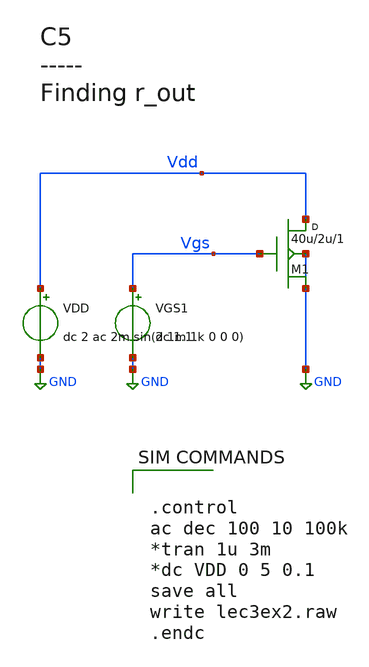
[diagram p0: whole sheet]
** sch_path: lec3ex2.sch
**.subckt lec3ex2
M1 Vdd Vgs GND GND NMOS w=40u l=2u m=1
VGS1 Vgs GND dc 1.1
VDD Vdd GND dc 2 ac 2m sin(2 1m 1k 0 0 0)
**** begin user architecture code


.control
ac dec 100 10 100k
*tran 1u 3m
*dc VDD 0 5 0.1
save all
write lec3ex2.raw
.endc




*

* Long channel models from CMOS Circuit Design, Layout, and Simulation,

* Level=3 models VDD=5V, see CMOSedu.com

*

.MODEL N_1u NMOS LEVEL  = 3
  TOX    = 200E-10         NSUB   = 1E17            GAMMA  = 0.5
  PHI    = 0.7             VTO    = 0.8             DELTA  = 3.0
  UO     = 650             ETA    = 3.0E-6          THETA  = 0.1
  KP     = 120E-6          VMAX   = 1E5             KAPPA  = 0.3
  RSH    = 0               NFS    = 1E12            TPG    = 1
  XJ     = 500E-9          LD     = 100E-9
  CGDO   = 200E-12         CGSO   = 200E-12         CGBO   = 1E-10
  CJ     = 400E-6          PB     = 1               MJ     = 0.5
  CJSW   = 300E-12         MJSW   = 0.5

*

.MODEL P_1u PMOS LEVEL  = 3
  TOX    = 200E-10         NSUB   = 1E17            GAMMA  = 0.6
  PHI    = 0.7             VTO    = -0.9            DELTA  = 0.1
  UO     = 250             ETA    = 0               THETA  = 0.1
  KP     = 40E-6           VMAX   = 5E4             KAPPA  = 1
  RSH    = 0               NFS    = 1E12            TPG    = -1
  XJ     = 500E-9          LD     = 100E-9
  CGDO   = 200E-12         CGSO   = 200E-12         CGBO   = 1E-10
  CJ     = 400E-6          PB     = 1               MJ     = 0.5
  CJSW   = 300E-12         MJSW   = 0.5

*

*

* Short channel models from CMOS Circuit Design, Layout, and Simulation,

* 50nm BSIM4 models VDD=1V, see CMOSedu.com

*

.model  N_50n  nmos  level = 54
 binunit = 1            paramchk= 1            mobmod  = 0
 capmod  = 2            igcmod  = 1            igbmod  = 1            geomod  = 0
 diomod  = 1            rdsmod  = 0            rbodymod= 1            rgatemod= 1
 permod  = 1            acnqsmod= 0            trnqsmod= 0
 tnom    = 27           toxe    = 1.4e-009     toxp    = 7e-010       toxm    = 1.4e-009
 epsrox  = 3.9          wint    = 5e-009       lint    = 1.2e-008
 ll      = 0            wl      = 0            lln     = 1            wln     = 1
 lw      = 0            ww      = 0            lwn     = 1            wwn     = 1
 lwl     = 0            wwl     = 0            xpart   = 0            toxref  = 1.4e-009
 vth0    = 0.22         k1      = 0.35         k2      = 0.05         k3      = 0
 k3b     = 0            w0      = 2.5e-006     dvt0    = 2.8          dvt1    = 0.52
 dvt2    = -0.032       dvt0w   = 0            dvt1w   = 0            dvt2w   = 0
 dsub    = 2            minv    = 0.05         voffl   = 0            dvtp0   = 1e-007
 dvtp1   = 0.05         lpe0    = 5.75e-008    lpeb    = 2.3e-010     xj      = 2e-008
 ngate   = 5e+020       ndep    = 2.8e+018     nsd     = 1e+020       phin    = 0
 cdsc    = 0.0002       cdscb   = 0            cdscd   = 0            cit     = 0
 voff    = -0.15        nfactor = 1.2          eta0    = 0.15         etab    = 0
 vfb     = -0.55        u0      = 0.032        ua      = 1.6e-010     ub      = 1.1e-017
 uc      = -3e-011      vsat    = 1.1e+005     a0      = 2            ags     = 1e-020
 a1      = 0            a2      = 1            b0      = -1e-020      b1      = 0
 keta    = 0.04         dwg     = 0            dwb     = 0            pclm    = 0.18
 pdiblc1 = 0.028        pdiblc2 = 0.022        pdiblcb = -0.005       drout   = 0.45
 pvag    = 1e-020       delta   = 0.01         pscbe1  = 8.14e+008    pscbe2  = 1e-007
 fprout  = 0.2          pdits   = 0.2          pditsd  = 0.23         pditsl  = 2.3e+006
 rsh     = 3            rdsw    = 150          rsw     = 150          rdw     = 150
 rdswmin = 0            rdwmin  = 0            rswmin  = 0            prwg    = 0
 prwb    = 6.8e-011     wr      = 1            alpha0  = 0.074        alpha1  = 0.005
 beta0   = 30           agidl   = 0.0002       bgidl   = 2.1e+009     cgidl   = 0.0002
 egidl   = 0.8
 aigbacc = 0.012        bigbacc = 0.0028       cigbacc = 0.002
 nigbacc = 1            aigbinv = 0.014        bigbinv = 0.004        cigbinv = 0.004
 eigbinv = 1.1          nigbinv = 3            aigc    = 0.017        bigc    = 0.0028
 cigc    = 0.002        aigsd   = 0.017        bigsd   = 0.0028       cigsd   = 0.002
 nigc    = 1            poxedge = 1            pigcd   = 1            ntox    = 1
 xrcrg1  = 12           xrcrg2  = 5
 cgso    = 6.238e-010   cgdo    = 6.238e-010   cgbo    = 2.56e-011    cgdl    = 2.495e-10
 cgsl    = 2.495e-10    ckappas = 0.02         ckappad = 0.02         acde    = 1
 moin    = 15           noff    = 0.9          voffcv  = 0.02
 kt1     = -0.21        kt1l    = 0.0           kt2     = -0.042        ute     = -1.5
 ua1     = 1e-009       ub1     = -3.5e-019     uc1     = 0             prt     = 0
 at      = 53000
 fnoimod = 1            tnoimod = 0
 jss     = 0.0001       jsws    = 1e-011       jswgs   = 1e-010       njs     = 1
 ijthsfwd= 0.01         ijthsrev= 0.001        bvs     = 10           xjbvs   = 1
 jsd     = 0.0001       jswd    = 1e-011       jswgd   = 1e-010       njd     = 1
 ijthdfwd= 0.01         ijthdrev= 0.001        bvd     = 10           xjbvd   = 1
 pbs     = 1            cjs     = 0.0005       mjs     = 0.5          pbsws   = 1
 cjsws   = 5e-010       mjsws   = 0.33         pbswgs  = 1            cjswgs  = 5e-010
 mjswgs  = 0.33         pbd     = 1            cjd     = 0.0005       mjd     = 0.5
 pbswd   = 1            cjswd   = 5e-010       mjswd   = 0.33         pbswgd  = 1
 cjswgd  = 5e-010       mjswgd  = 0.33         tpb     = 0.005        tcj     = 0.001
 tpbsw   = 0.005        tcjsw   = 0.001        tpbswg  = 0.005        tcjswg  = 0.001
 xtis    = 3            xtid    = 3
 dmcg    = 0e-006       dmci    = 0e-006       dmdg    = 0e-006       dmcgt   = 0e-007
 dwj     = 0e-008     	xgw     = 0e-007       xgl     = 0e-008
 rshg    = 0.4          gbmin   = 1e-010       rbpb    = 5            rbpd    = 15
 rbps    = 15           rbdb    = 15           rbsb    = 15           ngcon   = 1

*

.model  P_50n  pmos  level = 54
 binunit = 1            paramchk= 1            mobmod  = 0
 capmod  = 2            igcmod  = 1            igbmod  = 1            geomod  = 0
 diomod  = 1            rdsmod  = 0            rbodymod= 1            rgatemod= 1
 permod  = 1            acnqsmod= 0            trnqsmod= 0
 tnom    = 27           toxe    = 1.4e-009     toxp    = 7e-010       toxm    = 1.4e-009
 epsrox  = 3.9          wint    = 5e-009       lint    = 1.2e-008
 ll      = 0            wl      = 0            lln     = 1            wln     = 1
 lw      = 0            ww      = 0            lwn     = 1            wwn     = 1
 lwl     = 0            wwl     = 0            xpart   = 0            toxref  = 1.4e-009
 vth0    = -0.22        k1      = 0.39         k2      = 0.05         k3      = 0
 k3b     = 0            w0      = 2.5e-006     dvt0    = 3.9          dvt1    = 0.635
 dvt2    = -0.032       dvt0w   = 0            dvt1w   = 0            dvt2w   = 0
 dsub    = 0.7          minv    = 0.05         voffl   = 0            dvtp0   = 0.5e-008
 dvtp1   = 0.05         lpe0    = 5.75e-008    lpeb    = 2.3e-010     xj      = 2e-008
 ngate   = 5e+020       ndep    = 2.8e+018     nsd     = 1e+020       phin    = 0
 cdsc    = 0.000258     cdscb   = 0            cdscd   = 6.1e-008     cit     = 0
 voff    = -0.15        nfactor = 2            eta0    = 0.15         etab    = 0
 vfb     = 0.55         u0      = 0.0095       ua      = 1.6e-009     ub      = 8e-018
 uc      = 4.6e-013     vsat    = 90000        a0      = 1.2          ags     = 1e-020
 a1      = 0            a2      = 1            b0      = -1e-020      b1      = 0
 keta    = -0.047       dwg     = 0            dwb     = 0            pclm    = 0.55
 pdiblc1 = 0.03         pdiblc2 = 0.0055       pdiblcb = 3.4e-008     drout   = 0.56
 pvag    = 1e-020       delta   = 0.014        pscbe1  = 8.14e+008    pscbe2  = 9.58e-007
 fprout  = 0.2          pdits   = 0.2          pditsd  = 0.23         pditsl  = 2.3e+006
 rsh     = 3            rdsw    = 250          rsw     = 160          rdw     = 160
 rdswmin = 0            rdwmin  = 0            rswmin  = 0            prwg    = 3.22e-008
 prwb    = 6.8e-011     wr      = 1            alpha0  = 0.074        alpha1  = 0.005
 beta0   = 30           agidl   = 0.0002       bgidl   = 2.1e+009     cgidl   = 0.0002
 egidl   = 0.8
 aigbacc = 0.012        bigbacc = 0.0028       cigbacc = 0.002
 nigbacc = 1            aigbinv = 0.014        bigbinv = 0.004        cigbinv = 0.004
 eigbinv = 1.1          nigbinv = 3            aigc    = 0.69         bigc    = 0.0012
 cigc    = 0.0008       aigsd   = 0.0087       bigsd   = 0.0012       cigsd   = 0.0008
 nigc    = 1            poxedge = 1            pigcd   = 1            ntox    = 1
 xrcrg1  = 12           xrcrg2  = 5
 cgso    = 7.43e-010    cgdo    = 7.43e-010    cgbo    = 2.56e-011    cgdl    = 1e-014
 cgsl    = 1e-014       ckappas = 0.5          ckappad = 0.5          acde    = 1
 moin    = 15           noff    = 0.9          voffcv  = 0.02
 kt1     = -0.19        kt1l    = 0            kt2     = -0.052        ute     = -1.5
 ua1     = -1e-009      ub1     = 2e-018       uc1     = 0             prt     = 0
 at      = 33000
 fnoimod = 1            tnoimod = 0
 jss     = 0.0001       jsws    = 1e-011       jswgs   = 1e-010       njs     = 1
 ijthsfwd= 0.01         ijthsrev= 0.001        bvs     = 10           xjbvs   = 1
 jsd     = 0.0001       jswd    = 1e-011       jswgd   = 1e-010       njd     = 1
 ijthdfwd= 0.01         ijthdrev= 0.001        bvd     = 10           xjbvd   = 1
 pbs     = 1            cjs     = 0.0005       mjs     = 0.5          pbsws   = 1
 cjsws   = 5e-010       mjsws   = 0.33         pbswgs  = 1            cjswgs  = 5e-010
 mjswgs  = 0.33         pbd     = 1            cjd     = 0.0005       mjd     = 0.5
 pbswd   = 1            cjswd   = 5e-010       mjswd   = 0.33         pbswgd  = 1
 cjswgd  = 5e-010       mjswgd  = 0.33         tpb     = 0.005        tcj     = 0.001
 tpbsw   = 0.005        tcjsw   = 0.001        tpbswg  = 0.005        tcjswg  = 0.001
 xtis    = 3            xtid    = 3
 dmcg    = 0e-006       dmci    = 0e-006       dmdg    = 0e-006       dmcgt   = 0e-007
 dwj     = 0e-008     	xgw     = 0e-007       xgl     = 0e-008
 rshg    = 0.4          gbmin   = 1e-010       rbpb    = 5            rbpd    = 15
 rbps    = 15           rbdb    = 15           rbsb    = 15           ngcon   = 1




* BSIM3 models for AMI Semiconductor's C5 process
*
* Don't forget the .options scale=300nm if using drawn lengths
* and the MOSIS SUBM design rules
*
* 2<Ldrawn<500   10<Wdrawn<10000 Vdd=5V
* Note minimum L is 0.6 um while minimum W is 3 um
* Change to level=49 when using HSPICE or SmartSpice

.MODEL NMOS NMOS (                                 LEVEL   = 8 VERSION = 3.1            TNOM    = 27
+             TOX     = 1.39E-8 XJ      = 1.5E-7         NCH     = 1.7E17         VTH0    = 0.6696061 K1      =
+ 0.8351612      K2      = -0.0839158     K3      = 23.1023856 K3B     = -7.6841108     W0      = 1E-8
+           NLX     = 1E-9 DVT0W   = 0              DVT1W   = 0              DVT2W   = 0 DVT0    = 2.9047241
+      DVT1    = 0.4302695      DVT2    = -0.134857 U0      = 458.439679     UA      = 1E-13          UB      =
+ 1.485499E-18 UC      = 1.629939E-11   VSAT    = 1.643993E5     A0      = 0.6103537 AGS     = 0.1194608      B0
+      = 2.674756E-6    B1      = 5E-6 KETA    = -2.640681E-3   A1      = 8.219585E-5    A2      = 0.3564792
+ RDSW    = 1.387108E3     PRWG    = 0.0299916      PRWB    = 0.0363981 WR      = 1              WINT    =
+ 2.472348E-7    LINT    = 3.597605E-8 XL      = 0              XW      = 0              DWG     = -1.287163E-8
+ DWB     = 5.306586E-8    VOFF    = 0              NFACTOR = 0.8365585 CIT     = 0              CDSC
+    = 2.4E-4         CDSCD   = 0 CDSCB   = 0              ETA0    = 0.0246738      ETAB    = -1.406123E-3
+ DSUB    = 0.2543458      PCLM    = 2.5945188      PDIBLC1 = -0.4282336 PDIBLC2 = 2.311743E-3    PDIBLCB
+ = -0.0272914     DROUT   = 0.7283566 PSCBE1  = 5.598623E8     PSCBE2  = 5.461645E-5    PVAG    = 0
+ DELTA   = 0.01           RSH     = 81.8           MOBMOD  = 1 PRT     = 8.621          UTE     = -1
+             KT1     = -0.2501 KT1L    = -2.58E-9       KT2     = 0              UA1     = 5.4E-10 UB1     =
+ -4.8E-19       UC1     = -7.5E-11       AT      = 1E5 WL      = 0              WLN     = 1              WW
+      = 0 WWN     = 1              WWL     = 0              LL      = 0 LLN     = 1              LW      =
+ 0              LWN     = 1 LWL     = 0              CAPMOD  = 2              XPART   = 0.5 CGDO    =
+ 2E-10          CGSO    = 2E-10          CGBO    = 1E-9 CJ      = 4.197772E-4    PB      = 0.99
+           MJ      = 0.4515044 CJSW    = 3.242724E-10   PBSW    = 0.1            MJSW    = 0.1153991 CJSWG   =
+ 1.64E-10       PBSWG   = 0.1            MJSWG   = 0.1153991 CF      = 0              PVTH0   = 0.0585501
+      PRDSW   = 133.285505 PK2     = -0.0299638     WKETA   = -0.0248758     LKETA   = 1.173187E-3 AF      = 1
+              KF      = 0)
*
.MODEL PMOS PMOS (                                 LEVEL   = 8 VERSION = 3.1            TNOM    = 27
+             TOX     = 1.39E-8 XJ      = 1.5E-7         NCH     = 1.7E17         VTH0    = -0.9214347 K1      =
+ 0.5553722      K2      = 8.763328E-3    K3      = 6.3063558 K3B     = -0.6487362     W0      = 1.280703E-8
+    NLX     = 2.593997E-8 DVT0W   = 0              DVT1W   = 0              DVT2W   = 0 DVT0    = 2.5131165
+      DVT1    = 0.5480536      DVT2    = -0.1186489 U0      = 212.0166131    UA      = 2.807115E-9    UB
+      = 1E-21 UC      = -5.82128E-11   VSAT    = 1.713601E5     A0      = 0.8430019 AGS     = 0.1328608
+      B0      = 7.117912E-7    B1      = 5E-6 KETA    = -3.674859E-3   A1      = 4.77502E-5     A2      =
+ 0.3 RDSW    = 2.837206E3     PRWG    = -0.0363908     PRWB    = -1.016722E-5 WR      = 1
+              WINT    = 2.838038E-7    LINT    = 5.528807E-8 XL      = 0              XW      = 0              DWG
+     = -1.606385E-8 DWB     = 2.266386E-8    VOFF    = -0.0558512     NFACTOR = 0.9342488 CIT     = 0
+              CDSC    = 2.4E-4         CDSCD   = 0 CDSCB   = 0              ETA0    = 0.3251882      ETAB    =
+ -0.0580325 DSUB    = 1              PCLM    = 2.2409567      PDIBLC1 = 0.0411445 PDIBLC2 = 3.355575E-3
+    PDIBLCB = -0.0551797     DROUT   = 0.2036901 PSCBE1  = 6.44809E9      PSCBE2  = 6.300848E-10   PVAG    = 0
+ DELTA   = 0.01           RSH     = 101.6          MOBMOD  = 1 PRT     = 59.494         UTE     = -1
+             KT1     = -0.2942 KT1L    = 1.68E-9        KT2     = 0              UA1     = 4.5E-9 UB1     = -6.3E-18
+       UC1     = -1E-10         AT      = 1E3 WL      = 0              WLN     = 1              WW      = 0
+ WWN     = 1              WWL     = 0              LL      = 0 LLN     = 1              LW      = 0
+              LWN     = 1 LWL     = 0              CAPMOD  = 2              XPART   = 0.5 CGDO    = 2.9E-10
+        CGSO    = 2.9E-10        CGBO    = 1E-9 CJ      = 7.235528E-4    PB      = 0.9527355      MJ      =
+ 0.4955293 CJSW    = 2.692786E-10   PBSW    = 0.99           MJSW    = 0.2958392 CJSWG   = 6.4E-11
+        PBSWG   = 0.99           MJSWG   = 0.2958392 CF      = 0              PVTH0   = 5.98016E-3     PRDSW   =
+ 14.8598424 PK2     = 3.73981E-3     WKETA   = 5.292165E-3    LKETA   = -4.205905E-3  AF      = 1
+              KF      = 0)


**** end user architecture code
**.ends
.GLOBAL GND
.end
